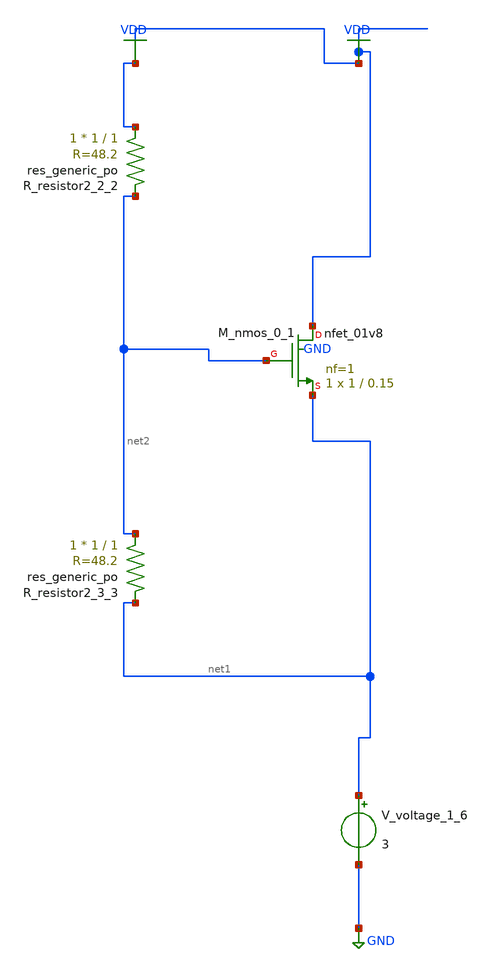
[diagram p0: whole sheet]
** sch_path: schematics/AMSNet/30.sch
**.subckt 30
XM_nmos_0_1 VDD net2 net1 GND sky130_fd_pr__nfet_01v8 L=0.15 W=1 nf=1 ad='int((1 + 1)/2) * 1 / 1 * 0.29'
+ as='int((1 + 2)/2) * 1 / 1 * 0.29' pd='2*int((1 + 1)/2) * (1 / 1 + 0.29)' ps='2*int((1 + 2)/2) * (1 / 1 + 0.29)'
+ nrd='0.29 / 1 ' nrs='0.29 / 1 ' sa=0 sb=0 sd=0 mult=1 m=1
XR_resistor2_2_2 VDD net2 sky130_fd_pr__res_generic_po W=1 L=1 m=1
XR_resistor2_3_3 net2 net1 sky130_fd_pr__res_generic_po W=1 L=1 m=1
V_voltage_1_6 net1 GND 3
**.ends
.GLOBAL GND
.GLOBAL VDD
.end
